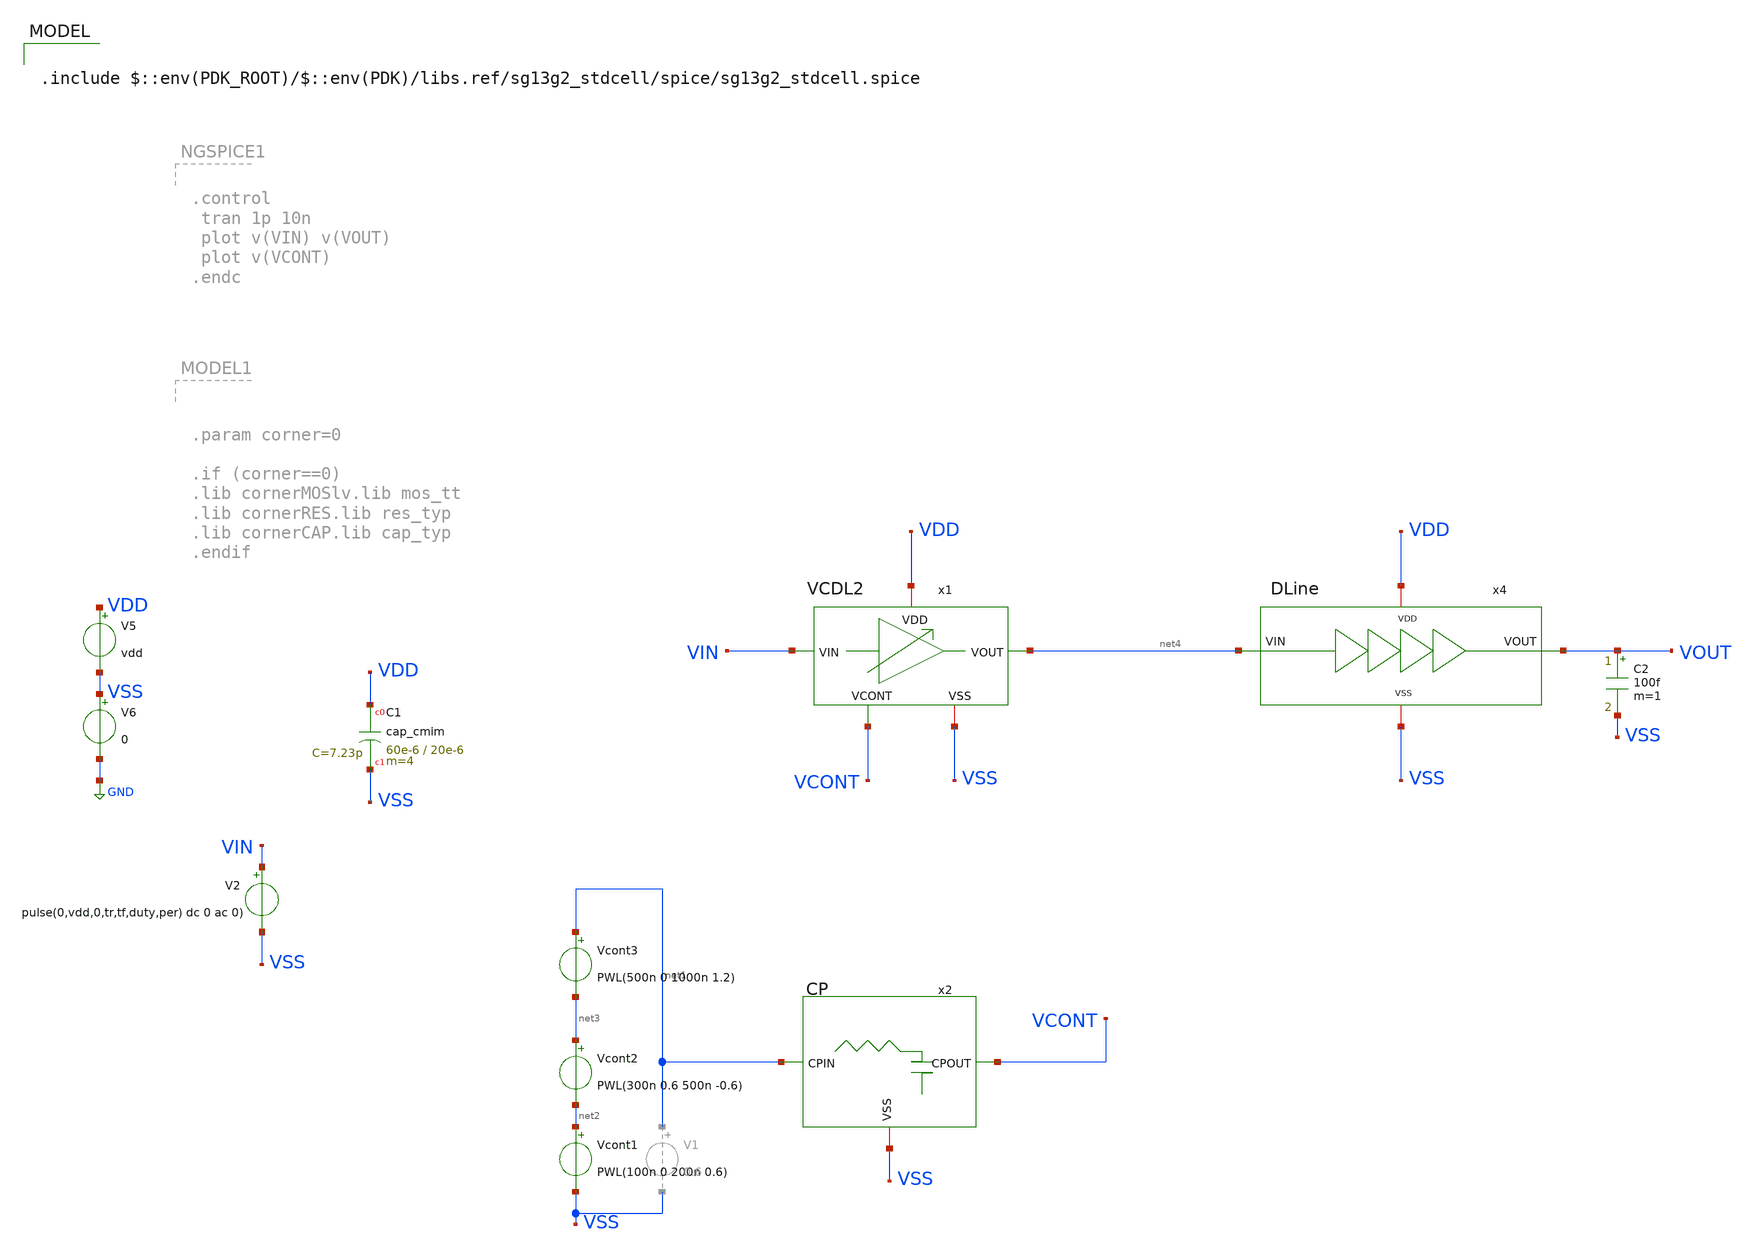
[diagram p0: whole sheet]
** sch_path: QDLL6501-main/schematic/xschem/testbenches/tb_VCDL2.sch
**.subckt tb_VCDL2
Vcont1 net2 VSS PWL(100n 0 200n 0.6)
x1 VDD VIN net4 VCONT VSS VCDL2
x2 net1 VCONT VSS CP
V2 VIN VSS pulse(0,vdd,0,tr,tf,duty,per) dc 0 ac 0)
V5 VDD VSS vdd
V6 VSS GND 0
x4 VSS VDD net4 VOUT DLine
C2 VOUT VSS 100f m=1
XC1 VDD VSS cap_cmim w=60e-6 l=20e-6 m=4 mm_ok=1
Vcont2 net3 net2 PWL(300n 0.6 500n -0.6)
Vcont3 net1 net3 PWL(500n 0 1000n 1.2)
**** begin user architecture code


.param temp=65 vdd=1.2
.param per=4n duty=2n tr=20p tf=20p delay=2n
.param vin=1.2 vd={vdd}
.options method=gear reltol=1e-1 abstol=1e-1 vntol=1e-1

.lib cornerMOSlv.lib mos_tt
.lib cornerCAP.lib cap_typ
.lib cornerRES.lib res_typ

* Ajustá TPER al período real de tu fuente (ej. 4n = 4 ns)
.param TPER = 4n

* Detectores de flanco ascendente (umbral 0.6 V para señal 0..1.2 V)
BTRIG_IN  TRIG_IN  0  V='(ddt(V(VIN))>0 && V(VIN)>0.6) ? 1 : 0'
BTRIG_OUT TRIG_OUT 0  V='(ddt(V(VOUT))>0 && V(VOUT)>0.6) ? 1 : 0'

* Sample-and-hold de tiempos de flanco (se guardan solo en el instante del flanco)
BIN_TIME  TIN   0  V='(V(TRIG_IN)>0 ? time : V(TIN))'
BOUT_TIME TOUT  0  V='(V(TRIG_OUT)>0 ? time : V(TOUT))'

* Retardo: solo se actualiza cuando TRIG_OUT se activa
BDELAY DELAY 0 V='(V(TRIG_OUT)>0 ? (V(TOUT)-V(TIN)) : V(DELAY))'

* Fase en grados (valor constante entre actualizaciones)
BPHASE PHASE 0 V='360*(V(DELAY)/TPER)'

* Inicializaciones para evitar valores indefinidos
.ic V(TIN)=0 V(TOUT)=0 V(DELAY)=0 V(PHASE)=0



.control
tran 1p 50n
plot v(VIN) v(VOUT)
plot i(V5)
plot v(PHASE)
.endc




.include $::env(PDK_ROOT)/$::env(PDK)/libs.ref/sg13g2_stdcell/spice/sg13g2_stdcell.spice

**** end user architecture code
**.ends
.GLOBAL GND
.end
